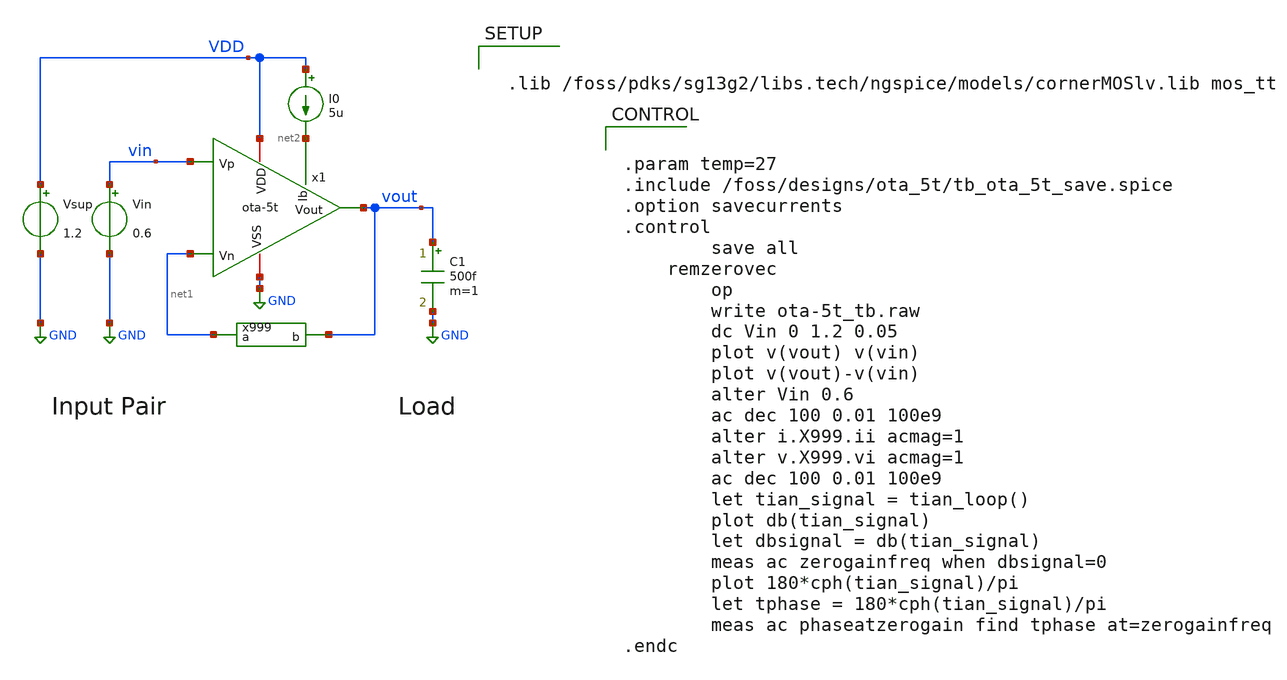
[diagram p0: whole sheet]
** sch_path: ota-5t_tb.sch
**.subckt ota-5t_tb
x1 vin net1 vout VDD GND net2 ota-5t
x999 net1 vout sub_x999
.subckt sub_x999 a b
Ii 0 x DC 0 AC 0
Vi x a DC 0 AC 1
Vnodebuffer b x 0
.ends loopgainprobe

.func tian_loop() {1/(1-1/(2*(ac1.I(v.X999.Vi)*ac2.V(X999.x)-ac1.V(X999.x)*ac2.I(v.X999.Vi))+ac1.V(X999.x)+ac2.I(v.X999.Vi)))}

C1 vout GND 500f m=1
Vin vin GND 0.6
Vsup VDD GND 1.2
I0 VDD net2 5u
**** begin user architecture code


 .lib /foss/pdks/sg13g2/libs.tech/ngspice/models/cornerMOSlv.lib mos_tt




.param temp=27
.include /foss/designs/ota_5t/tb_ota_5t_save.spice
.option savecurrents
.control
        save all
	remzerovec
        op
        write ota-5t_tb.raw
        dc Vin 0 1.2 0.05
        plot v(vout) v(vin)
        plot v(vout)-v(vin)
        alter Vin 0.6
        ac dec 100 0.01 100e9
        alter i.X999.ii acmag=1
        alter v.X999.vi acmag=1
        ac dec 100 0.01 100e9
        let tian_signal = tian_loop()
        plot db(tian_signal)
        let dbsignal = db(tian_signal)
        meas ac zerogainfreq when dbsignal=0
        plot 180*cph(tian_signal)/pi
        let tphase = 180*cph(tian_signal)/pi
        meas ac phaseatzerogain find tphase at=zerogainfreq
.endc


**** end user architecture code
**.ends

* expanding   symbol:  /foss/designs/ota_5t/ota-5t.sym # of pins=6
** sym_path: ota-5t.sym
** sch_path: ota-5t.sch
.subckt ota-5t Vp Vn Vout VDD VSS Ib
*.iopin VDD
*.ipin Vp
*.opin Vout
*.ipin Vn
*.iopin VSS
*.ipin Ib
Xm1a vs Vp vd VSS sg13_lv_nmos w=10u l=4u ng=1 m=4 mm_ok=1
Xm2b Vout vd VDD VDD sg13_lv_pmos w=4u l=1u ng=1 m=1 mm_ok=1
Xm2a vd vd VDD VDD sg13_lv_pmos w=4u l=1u ng=1 m=1 mm_ok=1
Xm3a VSS Ib vs VSS sg13_lv_nmos w=1u l=1u ng=1 m=2 mm_ok=1
Xm1b vs Vn Vout VSS sg13_lv_nmos w=10u l=4u ng=1 m=4 mm_ok=1
Xm3b VSS Ib Ib VSS sg13_lv_nmos w=1u l=1u ng=1 m=2 mm_ok=1
.ends

.GLOBAL GND
.end
